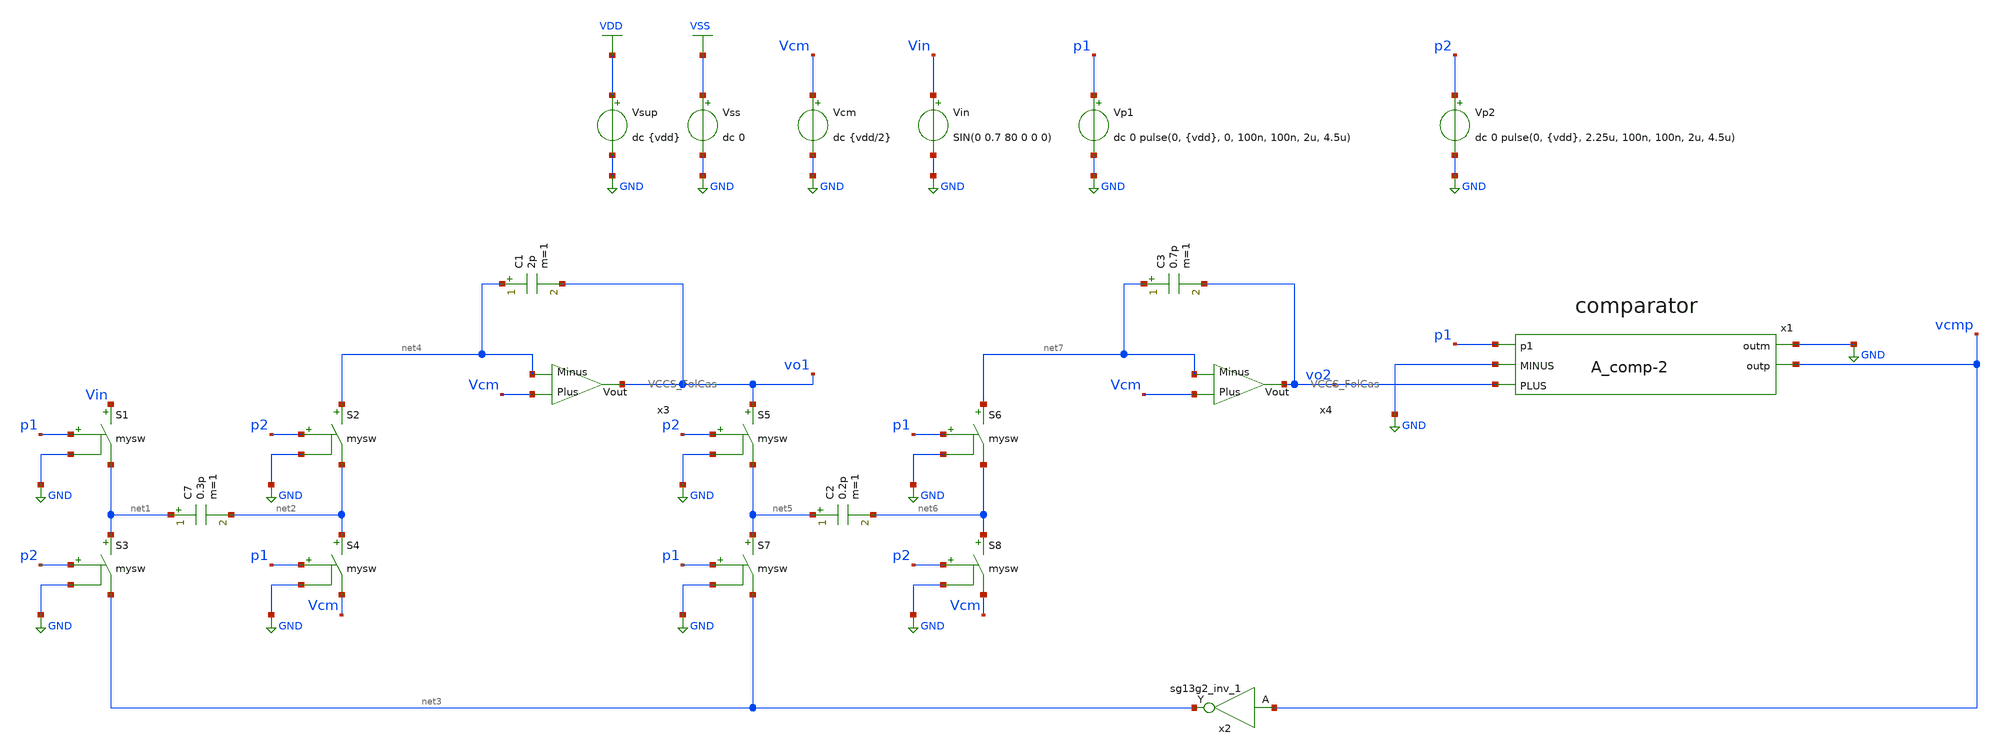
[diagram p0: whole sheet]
** sch_path: DSM/Schematics/Designs_Hrishi/RealCircuits/Real_DSM_Design.sch
**.subckt Real_DSM_Design
Vcm Vcm GND dc {vdd/2}
Vin Vin GND SIN(0 0.7 80 0 0 0)
S1 Vin net1 p1 GND mysw
S2 net4 net2 p2 GND mysw
S3 net1 net3 p2 GND mysw
S4 net2 Vcm p1 GND mysw
C7 net1 net2 0.3p m=1
C1 net4 vo1 2p m=1
S5 vo1 net5 p2 GND mysw
S6 net7 net6 p1 GND mysw
S7 net5 net3 p1 GND mysw
S8 net6 Vcm p2 GND mysw
C2 net5 net6 0.2p m=1
C3 net7 vo2 0.7p m=1
x2 net3 vcmp Vdd Vss sg13g2_inv_1
Vsup VDD GND dc {vdd}
Vss VSS GND dc 0
Vp1 p1 GND dc 0 pulse(0, {vdd}, 0, 100n, 100n, 2u, 4.5u)
Vp2 p2 GND dc 0 pulse(0, {vdd}, 2.25u, 100n, 100n, 2u, 4.5u)
x3 Vcm vo1 net4 VCCS_FolCas
x4 Vcm vo2 net7 VCCS_FolCas
x1 p1 GND vcmp GND vo2 A_comp-2
**** begin user architecture code

.lib $::SG13G2_MODELS/cornerMOSlv.lib mos_tt
.lib $::SG13G2_MODELS/cornerRES.lib res_typ
.inc /foss/pdks/sg13g2/libs.ref/sg13g2_stdcell/spice/sg13g2_stdcell.spice



.param temp=27 vdd = 1.5

.model mysw SW vt={vdd/2} ron=0.1
.option method=gear reltol=1e-4

.control
reset

run
tran 10n 60u
set color0 = white
set color1 = black
plot vo1 vo2

set wr_singlescale
set wr_vecnames
wrdata IDEAL_SwitchCap.txt vcmp p1 p2
.endc


**** end user architecture code
**.ends
.GLOBAL GND
.GLOBAL VDD
.GLOBAL VSS
.end
